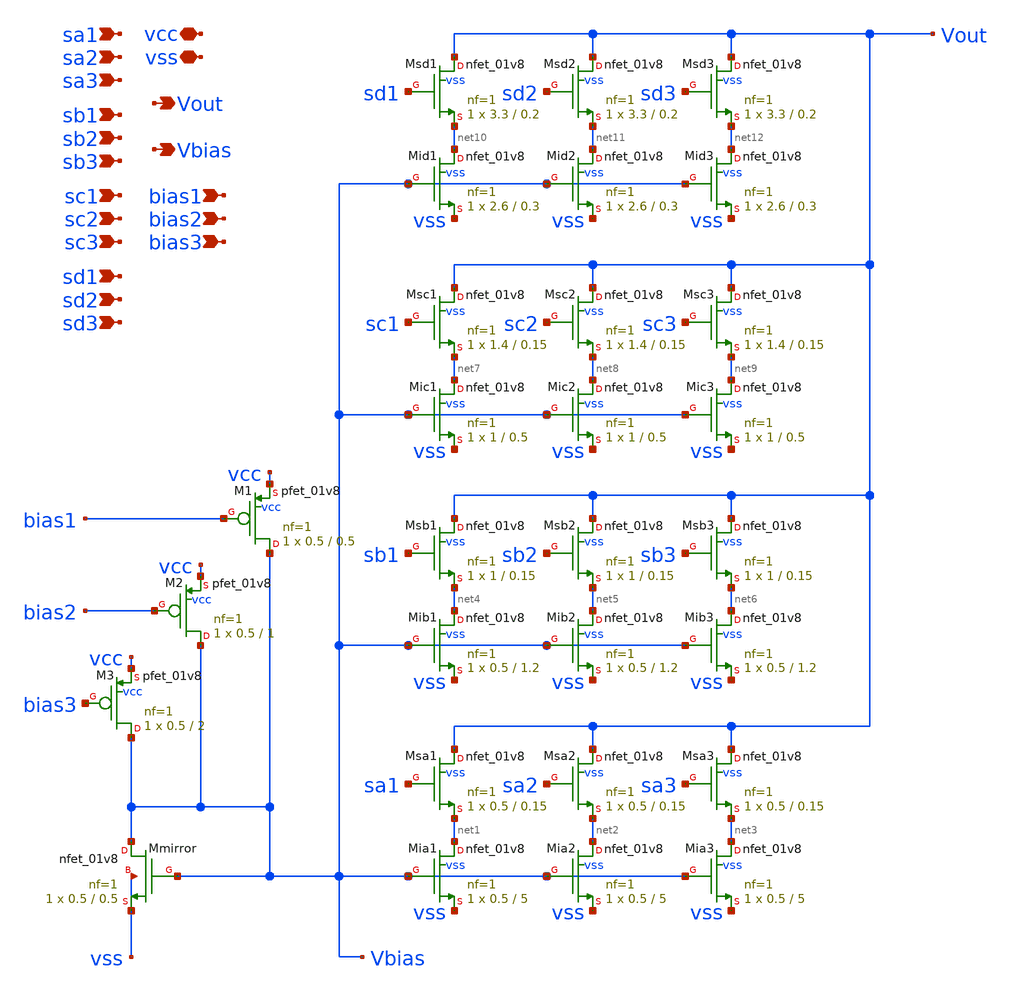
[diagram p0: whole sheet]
** sch_path: xschem/segdac.sch
**.subckt segdac vcc vss Vout Vbias sa1 sa2 sa3 sb1 sb2 sb3 sc1 sc2 sc3 sd1 sd2 sd3 bias1 bias2
*+ bias3
*.iopin vcc
*.iopin vss
*.opin Vout
*.opin Vbias
*.ipin sa1
*.ipin sa2
*.ipin sa3
*.ipin sb1
*.ipin sb2
*.ipin sb3
*.ipin sc1
*.ipin sc2
*.ipin sc3
*.ipin sd1
*.ipin sd2
*.ipin sd3
*.ipin bias1
*.ipin bias2
*.ipin bias3
XMmirror Vbias Vbias vss vss sky130_fd_pr__nfet_01v8 L=0.5 W=0.5 nf=1 ad='int((nf+1)/2) * W/nf * 0.29'
+ as='int((nf+2)/2) * W/nf * 0.29' pd='2*int((nf+1)/2) * (W/nf + 0.29)' ps='2*int((nf+2)/2) * (W/nf + 0.29)'
+ nrd='0.29 / W' nrs='0.29 / W' sa=0 sb=0 sd=0 mult=1 m=1
XMia1 net1 Vbias vss vss sky130_fd_pr__nfet_01v8 L=5 W=0.5 nf=1 ad='int((nf+1)/2) * W/nf * 0.29' as='int((nf+2)/2) * W/nf * 0.29'
+ pd='2*int((nf+1)/2) * (W/nf + 0.29)' ps='2*int((nf+2)/2) * (W/nf + 0.29)' nrd='0.29 / W' nrs='0.29 / W'
+ sa=0 sb=0 sd=0 mult=1 m=1
XMia2 net2 Vbias vss vss sky130_fd_pr__nfet_01v8 L=5 W=0.5 nf=1 ad='int((nf+1)/2) * W/nf * 0.29' as='int((nf+2)/2) * W/nf * 0.29'
+ pd='2*int((nf+1)/2) * (W/nf + 0.29)' ps='2*int((nf+2)/2) * (W/nf + 0.29)' nrd='0.29 / W' nrs='0.29 / W'
+ sa=0 sb=0 sd=0 mult=1 m=1
XMia3 net3 Vbias vss vss sky130_fd_pr__nfet_01v8 L=5 W=0.5 nf=1 ad='int((nf+1)/2) * W/nf * 0.29' as='int((nf+2)/2) * W/nf * 0.29'
+ pd='2*int((nf+1)/2) * (W/nf + 0.29)' ps='2*int((nf+2)/2) * (W/nf + 0.29)' nrd='0.29 / W' nrs='0.29 / W'
+ sa=0 sb=0 sd=0 mult=1 m=1
XMsa1 Vout sa1 net1 vss sky130_fd_pr__nfet_01v8 L=0.15 W=0.5 nf=1 ad='int((nf+1)/2) * W/nf * 0.29' as='int((nf+2)/2) * W/nf * 0.29'
+ pd='2*int((nf+1)/2) * (W/nf + 0.29)' ps='2*int((nf+2)/2) * (W/nf + 0.29)' nrd='0.29 / W' nrs='0.29 / W'
+ sa=0 sb=0 sd=0 mult=1 m=1
XMsa2 Vout sa2 net2 vss sky130_fd_pr__nfet_01v8 L=0.15 W=0.5 nf=1 ad='int((nf+1)/2) * W/nf * 0.29' as='int((nf+2)/2) * W/nf * 0.29'
+ pd='2*int((nf+1)/2) * (W/nf + 0.29)' ps='2*int((nf+2)/2) * (W/nf + 0.29)' nrd='0.29 / W' nrs='0.29 / W'
+ sa=0 sb=0 sd=0 mult=1 m=1
XMsa3 Vout sa3 net3 vss sky130_fd_pr__nfet_01v8 L=0.15 W=0.5 nf=1 ad='int((nf+1)/2) * W/nf * 0.29' as='int((nf+2)/2) * W/nf * 0.29'
+ pd='2*int((nf+1)/2) * (W/nf + 0.29)' ps='2*int((nf+2)/2) * (W/nf + 0.29)' nrd='0.29 / W' nrs='0.29 / W'
+ sa=0 sb=0 sd=0 mult=1 m=1
XMib1 net4 Vbias vss vss sky130_fd_pr__nfet_01v8 L=1.2 W=0.5 nf=1 ad='int((nf+1)/2) * W/nf * 0.29' as='int((nf+2)/2) * W/nf * 0.29'
+ pd='2*int((nf+1)/2) * (W/nf + 0.29)' ps='2*int((nf+2)/2) * (W/nf + 0.29)' nrd='0.29 / W' nrs='0.29 / W'
+ sa=0 sb=0 sd=0 mult=1 m=1
XMib2 net5 Vbias vss vss sky130_fd_pr__nfet_01v8 L=1.2 W=0.5 nf=1 ad='int((nf+1)/2) * W/nf * 0.29' as='int((nf+2)/2) * W/nf * 0.29'
+ pd='2*int((nf+1)/2) * (W/nf + 0.29)' ps='2*int((nf+2)/2) * (W/nf + 0.29)' nrd='0.29 / W' nrs='0.29 / W'
+ sa=0 sb=0 sd=0 mult=1 m=1
XMib3 net6 Vbias vss vss sky130_fd_pr__nfet_01v8 L=1.2 W=0.5 nf=1 ad='int((nf+1)/2) * W/nf * 0.29' as='int((nf+2)/2) * W/nf * 0.29'
+ pd='2*int((nf+1)/2) * (W/nf + 0.29)' ps='2*int((nf+2)/2) * (W/nf + 0.29)' nrd='0.29 / W' nrs='0.29 / W'
+ sa=0 sb=0 sd=0 mult=1 m=1
XMsb1 Vout sb1 net4 vss sky130_fd_pr__nfet_01v8 L=0.15 W=1 nf=1 ad='int((nf+1)/2) * W/nf * 0.29' as='int((nf+2)/2) * W/nf * 0.29'
+ pd='2*int((nf+1)/2) * (W/nf + 0.29)' ps='2*int((nf+2)/2) * (W/nf + 0.29)' nrd='0.29 / W' nrs='0.29 / W'
+ sa=0 sb=0 sd=0 mult=1 m=1
XMsb2 Vout sb2 net5 vss sky130_fd_pr__nfet_01v8 L=0.15 W=1 nf=1 ad='int((nf+1)/2) * W/nf * 0.29' as='int((nf+2)/2) * W/nf * 0.29'
+ pd='2*int((nf+1)/2) * (W/nf + 0.29)' ps='2*int((nf+2)/2) * (W/nf + 0.29)' nrd='0.29 / W' nrs='0.29 / W'
+ sa=0 sb=0 sd=0 mult=1 m=1
XMsb3 Vout sb3 net6 vss sky130_fd_pr__nfet_01v8 L=0.15 W=1 nf=1 ad='int((nf+1)/2) * W/nf * 0.29' as='int((nf+2)/2) * W/nf * 0.29'
+ pd='2*int((nf+1)/2) * (W/nf + 0.29)' ps='2*int((nf+2)/2) * (W/nf + 0.29)' nrd='0.29 / W' nrs='0.29 / W'
+ sa=0 sb=0 sd=0 mult=1 m=1
XMic1 net7 Vbias vss vss sky130_fd_pr__nfet_01v8 L=0.5 W=1 nf=1 ad='int((nf+1)/2) * W/nf * 0.29' as='int((nf+2)/2) * W/nf * 0.29'
+ pd='2*int((nf+1)/2) * (W/nf + 0.29)' ps='2*int((nf+2)/2) * (W/nf + 0.29)' nrd='0.29 / W' nrs='0.29 / W'
+ sa=0 sb=0 sd=0 mult=1 m=1
XMic2 net8 Vbias vss vss sky130_fd_pr__nfet_01v8 L=0.5 W=1 nf=1 ad='int((nf+1)/2) * W/nf * 0.29' as='int((nf+2)/2) * W/nf * 0.29'
+ pd='2*int((nf+1)/2) * (W/nf + 0.29)' ps='2*int((nf+2)/2) * (W/nf + 0.29)' nrd='0.29 / W' nrs='0.29 / W'
+ sa=0 sb=0 sd=0 mult=1 m=1
XMic3 net9 Vbias vss vss sky130_fd_pr__nfet_01v8 L=0.5 W=1 nf=1 ad='int((nf+1)/2) * W/nf * 0.29' as='int((nf+2)/2) * W/nf * 0.29'
+ pd='2*int((nf+1)/2) * (W/nf + 0.29)' ps='2*int((nf+2)/2) * (W/nf + 0.29)' nrd='0.29 / W' nrs='0.29 / W'
+ sa=0 sb=0 sd=0 mult=1 m=1
XMsc1 Vout sc1 net7 vss sky130_fd_pr__nfet_01v8 L=0.15 W=1.4 nf=1 ad='int((nf+1)/2) * W/nf * 0.29' as='int((nf+2)/2) * W/nf * 0.29'
+ pd='2*int((nf+1)/2) * (W/nf + 0.29)' ps='2*int((nf+2)/2) * (W/nf + 0.29)' nrd='0.29 / W' nrs='0.29 / W'
+ sa=0 sb=0 sd=0 mult=1 m=1
XMsc2 Vout sc2 net8 vss sky130_fd_pr__nfet_01v8 L=0.15 W=1.4 nf=1 ad='int((nf+1)/2) * W/nf * 0.29' as='int((nf+2)/2) * W/nf * 0.29'
+ pd='2*int((nf+1)/2) * (W/nf + 0.29)' ps='2*int((nf+2)/2) * (W/nf + 0.29)' nrd='0.29 / W' nrs='0.29 / W'
+ sa=0 sb=0 sd=0 mult=1 m=1
XMsc3 Vout sc3 net9 vss sky130_fd_pr__nfet_01v8 L=0.15 W=1.4 nf=1 ad='int((nf+1)/2) * W/nf * 0.29' as='int((nf+2)/2) * W/nf * 0.29'
+ pd='2*int((nf+1)/2) * (W/nf + 0.29)' ps='2*int((nf+2)/2) * (W/nf + 0.29)' nrd='0.29 / W' nrs='0.29 / W'
+ sa=0 sb=0 sd=0 mult=1 m=1
XMid1 net10 Vbias vss vss sky130_fd_pr__nfet_01v8 L=0.3 W=2.6 nf=1 ad='int((nf+1)/2) * W/nf * 0.29' as='int((nf+2)/2) * W/nf * 0.29'
+ pd='2*int((nf+1)/2) * (W/nf + 0.29)' ps='2*int((nf+2)/2) * (W/nf + 0.29)' nrd='0.29 / W' nrs='0.29 / W'
+ sa=0 sb=0 sd=0 mult=1 m=1
XMid2 net11 Vbias vss vss sky130_fd_pr__nfet_01v8 L=0.3 W=2.6 nf=1 ad='int((nf+1)/2) * W/nf * 0.29' as='int((nf+2)/2) * W/nf * 0.29'
+ pd='2*int((nf+1)/2) * (W/nf + 0.29)' ps='2*int((nf+2)/2) * (W/nf + 0.29)' nrd='0.29 / W' nrs='0.29 / W'
+ sa=0 sb=0 sd=0 mult=1 m=1
XMid3 net12 Vbias vss vss sky130_fd_pr__nfet_01v8 L=0.3 W=2.6 nf=1 ad='int((nf+1)/2) * W/nf * 0.29' as='int((nf+2)/2) * W/nf * 0.29'
+ pd='2*int((nf+1)/2) * (W/nf + 0.29)' ps='2*int((nf+2)/2) * (W/nf + 0.29)' nrd='0.29 / W' nrs='0.29 / W'
+ sa=0 sb=0 sd=0 mult=1 m=1
XMsd1 Vout sd1 net10 vss sky130_fd_pr__nfet_01v8 L=0.2 W=3.3 nf=1 ad='int((nf+1)/2) * W/nf * 0.29' as='int((nf+2)/2) * W/nf * 0.29'
+ pd='2*int((nf+1)/2) * (W/nf + 0.29)' ps='2*int((nf+2)/2) * (W/nf + 0.29)' nrd='0.29 / W' nrs='0.29 / W'
+ sa=0 sb=0 sd=0 mult=1 m=1
XMsd2 Vout sd2 net11 vss sky130_fd_pr__nfet_01v8 L=0.2 W=3.3 nf=1 ad='int((nf+1)/2) * W/nf * 0.29' as='int((nf+2)/2) * W/nf * 0.29'
+ pd='2*int((nf+1)/2) * (W/nf + 0.29)' ps='2*int((nf+2)/2) * (W/nf + 0.29)' nrd='0.29 / W' nrs='0.29 / W'
+ sa=0 sb=0 sd=0 mult=1 m=1
XMsd3 Vout sd3 net12 vss sky130_fd_pr__nfet_01v8 L=0.2 W=3.3 nf=1 ad='int((nf+1)/2) * W/nf * 0.29' as='int((nf+2)/2) * W/nf * 0.29'
+ pd='2*int((nf+1)/2) * (W/nf + 0.29)' ps='2*int((nf+2)/2) * (W/nf + 0.29)' nrd='0.29 / W' nrs='0.29 / W'
+ sa=0 sb=0 sd=0 mult=1 m=1
XM1 Vbias bias1 vcc vcc sky130_fd_pr__pfet_01v8 L=0.5 W=0.5 nf=1 ad='int((nf+1)/2) * W/nf * 0.29' as='int((nf+2)/2) * W/nf * 0.29'
+ pd='2*int((nf+1)/2) * (W/nf + 0.29)' ps='2*int((nf+2)/2) * (W/nf + 0.29)' nrd='0.29 / W' nrs='0.29 / W'
+ sa=0 sb=0 sd=0 mult=1 m=1
XM2 Vbias bias2 vcc vcc sky130_fd_pr__pfet_01v8 L=1 W=0.5 nf=1 ad='int((nf+1)/2) * W/nf * 0.29' as='int((nf+2)/2) * W/nf * 0.29'
+ pd='2*int((nf+1)/2) * (W/nf + 0.29)' ps='2*int((nf+2)/2) * (W/nf + 0.29)' nrd='0.29 / W' nrs='0.29 / W'
+ sa=0 sb=0 sd=0 mult=1 m=1
XM3 Vbias bias3 vcc vcc sky130_fd_pr__pfet_01v8 L=2 W=0.5 nf=1 ad='int((nf+1)/2) * W/nf * 0.29' as='int((nf+2)/2) * W/nf * 0.29'
+ pd='2*int((nf+1)/2) * (W/nf + 0.29)' ps='2*int((nf+2)/2) * (W/nf + 0.29)' nrd='0.29 / W' nrs='0.29 / W'
+ sa=0 sb=0 sd=0 mult=1 m=1
**.ends
.end
